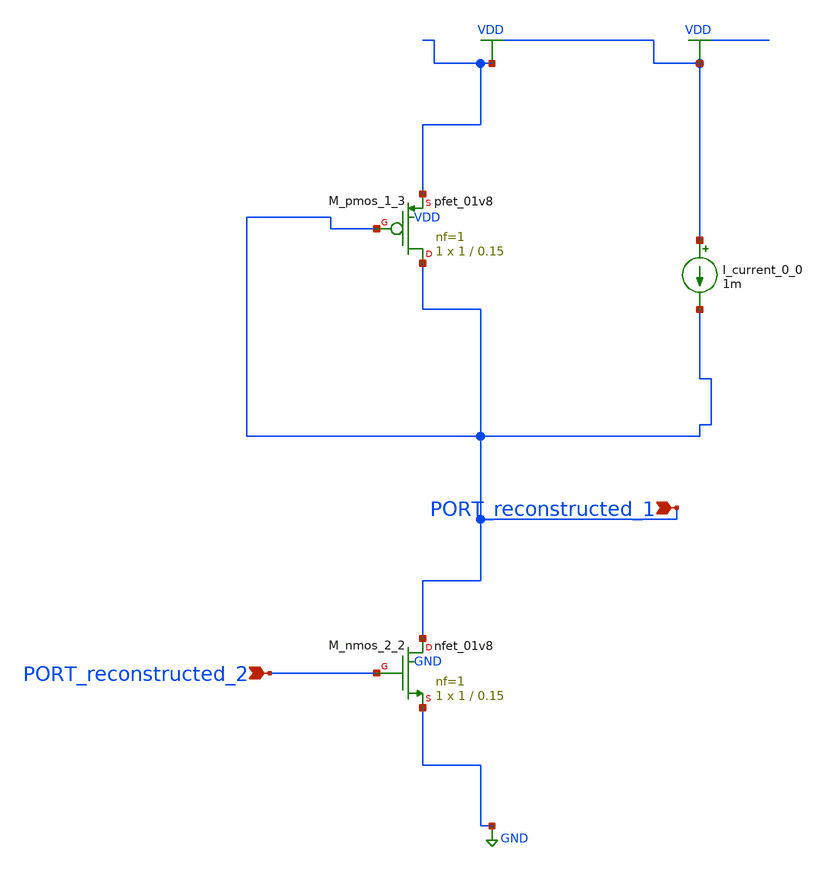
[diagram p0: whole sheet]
** sch_path: schematics/AMSNet/252.sch
**.subckt 252 PORT_reconstructed_1 PORT_reconstructed_2
*.ipin PORT_reconstructed_1
*.ipin PORT_reconstructed_2
I_current_0_0 VDD PORT_reconstructed_1 1m
XM_nmos_2_2 PORT_reconstructed_1 PORT_reconstructed_2 GND GND sky130_fd_pr__nfet_01v8 L=0.15 W=1 nf=1
+ ad='int((1 + 1)/2) * 1 / 1 * 0.29' as='int((1 + 2)/2) * 1 / 1 * 0.29' pd='2*int((1 + 1)/2) * (1 / 1 + 0.29)'
+ ps='2*int((1 + 2)/2) * (1 / 1 + 0.29)' nrd='0.29 / 1 ' nrs='0.29 / 1 ' sa=0 sb=0 sd=0 mult=1 m=1
XM_pmos_1_3 PORT_reconstructed_1 PORT_reconstructed_1 VDD VDD sky130_fd_pr__pfet_01v8 L=0.15 W=1 nf=1
+ ad='int((1 + 1)/2) * 1 / 1 * 0.29' as='int((1 + 2)/2) * 1 / 1 * 0.29' pd='2*int((1 + 1)/2) * (1 / 1 + 0.29)'
+ ps='2*int((1 + 2)/2) * (1 / 1 + 0.29)' nrd='0.29 / 1 ' nrs='0.29 / 1 ' sa=0 sb=0 sd=0 mult=1 m=1
**.ends
.GLOBAL GND
.GLOBAL VDD
.end
